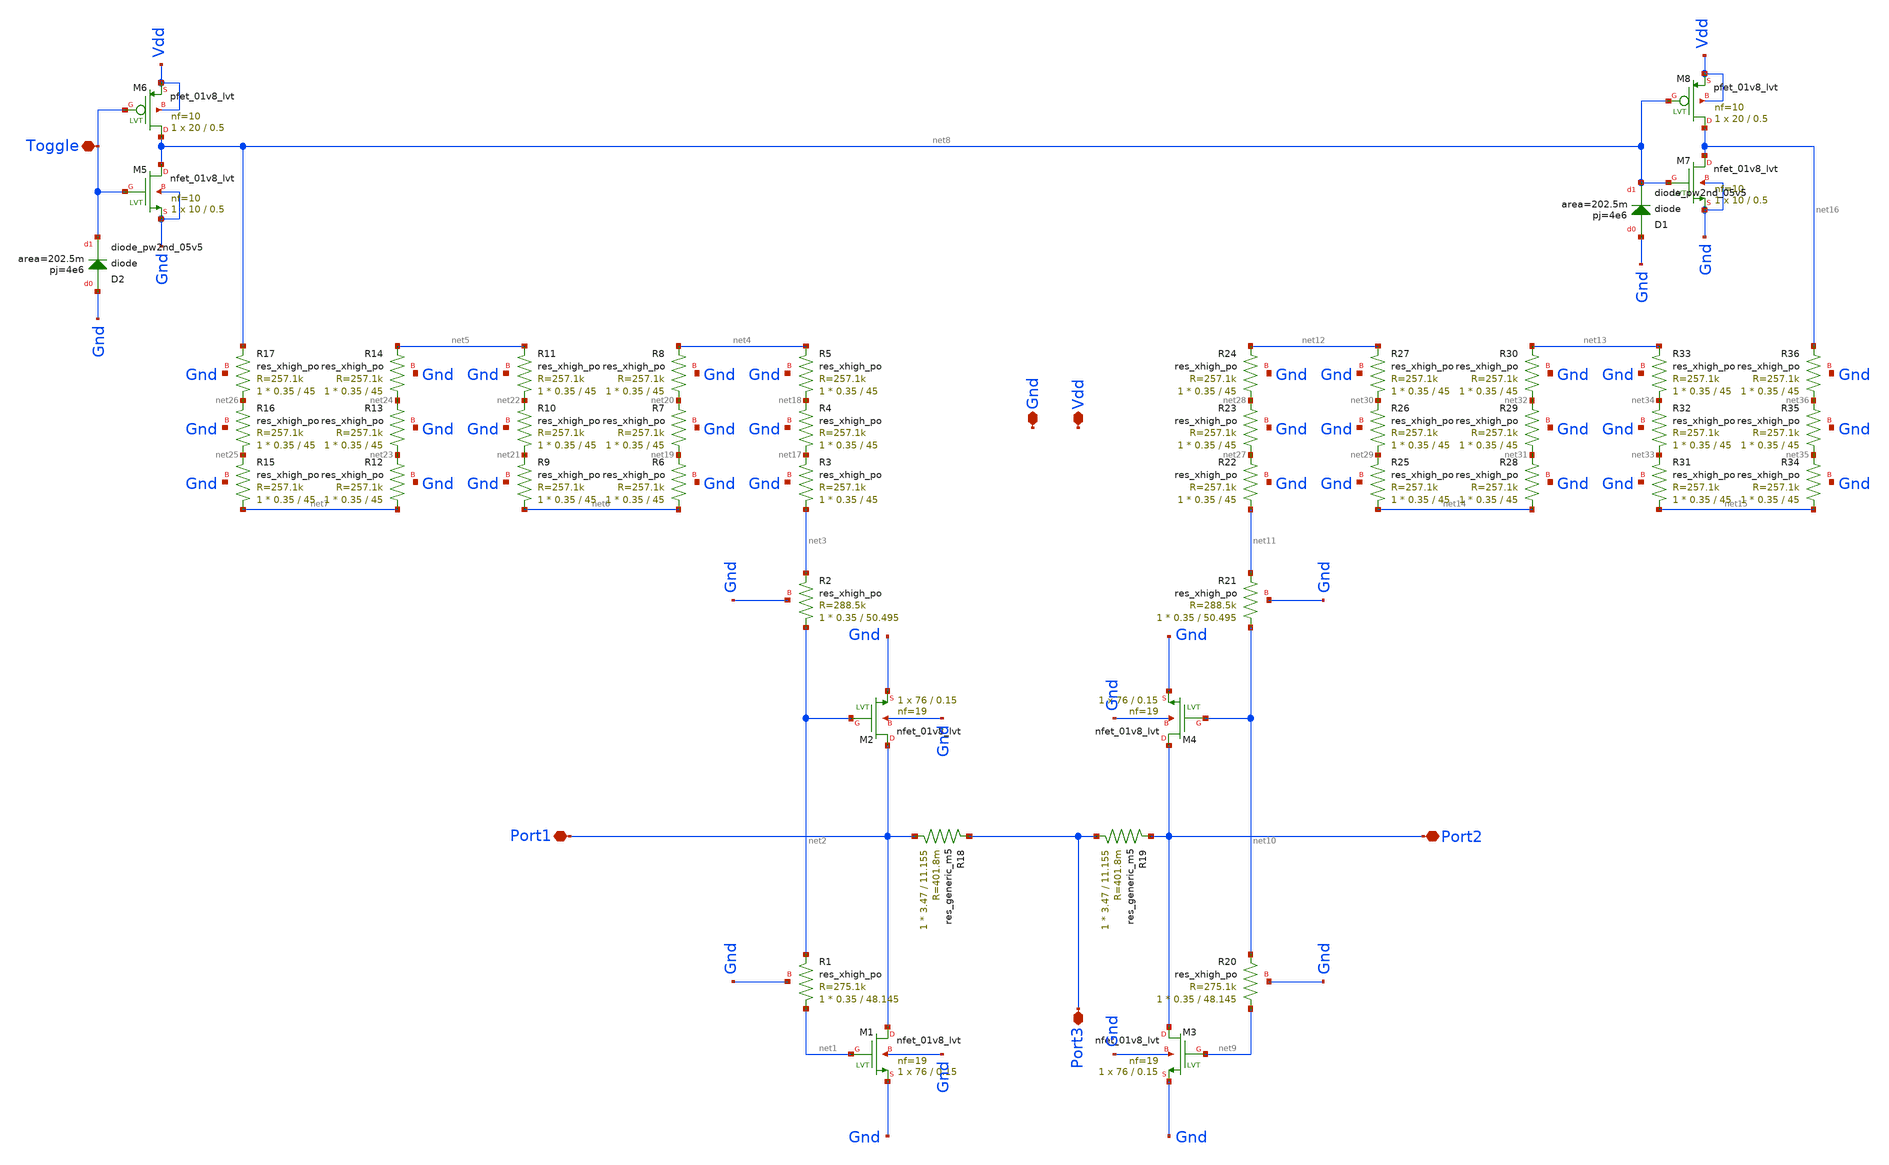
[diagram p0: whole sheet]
** sch_path: Switch_tapeout/xschem/RF_switch.sch
**.subckt RF_switch Port1 Port2 Port3 Toggle Vdd Gnd
*.iopin Port1
*.iopin Port2
*.iopin Port3
*.iopin Toggle
*.iopin Vdd
*.iopin Gnd
XM1 Port1 net1 Gnd Gnd sky130_fd_pr__nfet_01v8_lvt L=0.15 W=76 nf=19 ad='int((nf+1)/2) * W/nf * 0.29'
+ as='int((nf+2)/2) * W/nf * 0.29' pd='2*int((nf+1)/2) * (W/nf + 0.29)' ps='2*int((nf+2)/2) * (W/nf + 0.29)'
+ nrd='0.29 / W' nrs='0.29 / W' sa=0 sb=0 sd=0 mult=1 m=1
XR1 net1 net2 Gnd sky130_fd_pr__res_xhigh_po W=0.35 L=48.145 mult=1 m=1
XM2 Port1 net2 Gnd Gnd sky130_fd_pr__nfet_01v8_lvt L=0.15 W=76 nf=19 ad='int((nf+1)/2) * W/nf * 0.29'
+ as='int((nf+2)/2) * W/nf * 0.29' pd='2*int((nf+1)/2) * (W/nf + 0.29)' ps='2*int((nf+2)/2) * (W/nf + 0.29)'
+ nrd='0.29 / W' nrs='0.29 / W' sa=0 sb=0 sd=0 mult=1 m=1
XR2 net2 net3 Gnd sky130_fd_pr__res_xhigh_po W=0.35 L=50.495 mult=1 m=1
XR3 net3 net17 Gnd sky130_fd_pr__res_xhigh_po W=0.35 L=45 mult=1 m=1
XR4 net17 net18 Gnd sky130_fd_pr__res_xhigh_po W=0.35 L=45 mult=1 m=1
XR5 net18 net4 Gnd sky130_fd_pr__res_xhigh_po W=0.35 L=45 mult=1 m=1
XR6 net6 net19 Gnd sky130_fd_pr__res_xhigh_po W=0.35 L=45 mult=1 m=1
XR7 net19 net20 Gnd sky130_fd_pr__res_xhigh_po W=0.35 L=45 mult=1 m=1
XR8 net20 net4 Gnd sky130_fd_pr__res_xhigh_po W=0.35 L=45 mult=1 m=1
XR9 net6 net21 Gnd sky130_fd_pr__res_xhigh_po W=0.35 L=45 mult=1 m=1
XR10 net21 net22 Gnd sky130_fd_pr__res_xhigh_po W=0.35 L=45 mult=1 m=1
XR11 net22 net5 Gnd sky130_fd_pr__res_xhigh_po W=0.35 L=45 mult=1 m=1
XR12 net7 net23 Gnd sky130_fd_pr__res_xhigh_po W=0.35 L=45 mult=1 m=1
XR13 net23 net24 Gnd sky130_fd_pr__res_xhigh_po W=0.35 L=45 mult=1 m=1
XR14 net24 net5 Gnd sky130_fd_pr__res_xhigh_po W=0.35 L=45 mult=1 m=1
XR15 net7 net25 Gnd sky130_fd_pr__res_xhigh_po W=0.35 L=45 mult=1 m=1
XR16 net25 net26 Gnd sky130_fd_pr__res_xhigh_po W=0.35 L=45 mult=1 m=1
XR17 net26 net8 Gnd sky130_fd_pr__res_xhigh_po W=0.35 L=45 mult=1 m=1
XM3 Port2 net9 Gnd Gnd sky130_fd_pr__nfet_01v8_lvt L=0.15 W=76 nf=19 ad='int((nf+1)/2) * W/nf * 0.29'
+ as='int((nf+2)/2) * W/nf * 0.29' pd='2*int((nf+1)/2) * (W/nf + 0.29)' ps='2*int((nf+2)/2) * (W/nf + 0.29)'
+ nrd='0.29 / W' nrs='0.29 / W' sa=0 sb=0 sd=0 mult=1 m=1
XR20 net9 net10 Gnd sky130_fd_pr__res_xhigh_po W=0.35 L=48.145 mult=1 m=1
XM4 Port2 net10 Gnd Gnd sky130_fd_pr__nfet_01v8_lvt L=0.15 W=76 nf=19 ad='int((nf+1)/2) * W/nf * 0.29'
+ as='int((nf+2)/2) * W/nf * 0.29' pd='2*int((nf+1)/2) * (W/nf + 0.29)' ps='2*int((nf+2)/2) * (W/nf + 0.29)'
+ nrd='0.29 / W' nrs='0.29 / W' sa=0 sb=0 sd=0 mult=1 m=1
XR21 net10 net11 Gnd sky130_fd_pr__res_xhigh_po W=0.35 L=50.495 mult=1 m=1
XR22 net11 net27 Gnd sky130_fd_pr__res_xhigh_po W=0.35 L=45 mult=1 m=1
XR23 net27 net28 Gnd sky130_fd_pr__res_xhigh_po W=0.35 L=45 mult=1 m=1
XR24 net28 net12 Gnd sky130_fd_pr__res_xhigh_po W=0.35 L=45 mult=1 m=1
XR25 net14 net29 Gnd sky130_fd_pr__res_xhigh_po W=0.35 L=45 mult=1 m=1
XR26 net29 net30 Gnd sky130_fd_pr__res_xhigh_po W=0.35 L=45 mult=1 m=1
XR27 net30 net12 Gnd sky130_fd_pr__res_xhigh_po W=0.35 L=45 mult=1 m=1
XR28 net14 net31 Gnd sky130_fd_pr__res_xhigh_po W=0.35 L=45 mult=1 m=1
XR29 net31 net32 Gnd sky130_fd_pr__res_xhigh_po W=0.35 L=45 mult=1 m=1
XR30 net32 net13 Gnd sky130_fd_pr__res_xhigh_po W=0.35 L=45 mult=1 m=1
XR31 net15 net33 Gnd sky130_fd_pr__res_xhigh_po W=0.35 L=45 mult=1 m=1
XR32 net33 net34 Gnd sky130_fd_pr__res_xhigh_po W=0.35 L=45 mult=1 m=1
XR33 net34 net13 Gnd sky130_fd_pr__res_xhigh_po W=0.35 L=45 mult=1 m=1
XR34 net15 net35 Gnd sky130_fd_pr__res_xhigh_po W=0.35 L=45 mult=1 m=1
XR35 net35 net36 Gnd sky130_fd_pr__res_xhigh_po W=0.35 L=45 mult=1 m=1
XR36 net36 net16 Gnd sky130_fd_pr__res_xhigh_po W=0.35 L=45 mult=1 m=1
XM5 net8 Toggle Gnd Gnd sky130_fd_pr__nfet_01v8_lvt L=0.5 W=10 nf=10 ad='int((nf+1)/2) * W/nf * 0.29'
+ as='int((nf+2)/2) * W/nf * 0.29' pd='2*int((nf+1)/2) * (W/nf + 0.29)' ps='2*int((nf+2)/2) * (W/nf + 0.29)'
+ nrd='0.29 / W' nrs='0.29 / W' sa=0 sb=0 sd=0 mult=1 m=1
XM6 net8 Toggle Vdd Vdd sky130_fd_pr__pfet_01v8_lvt L=0.5 W=20 nf=10 ad='int((nf+1)/2) * W/nf * 0.29'
+ as='int((nf+2)/2) * W/nf * 0.29' pd='2*int((nf+1)/2) * (W/nf + 0.29)' ps='2*int((nf+2)/2) * (W/nf + 0.29)'
+ nrd='0.29 / W' nrs='0.29 / W' sa=0 sb=0 sd=0 mult=1 m=1
XM7 net16 net8 Gnd Gnd sky130_fd_pr__nfet_01v8_lvt L=0.5 W=10 nf=10 ad='int((nf+1)/2) * W/nf * 0.29'
+ as='int((nf+2)/2) * W/nf * 0.29' pd='2*int((nf+1)/2) * (W/nf + 0.29)' ps='2*int((nf+2)/2) * (W/nf + 0.29)'
+ nrd='0.29 / W' nrs='0.29 / W' sa=0 sb=0 sd=0 mult=1 m=1
XM8 net16 net8 Vdd Vdd sky130_fd_pr__pfet_01v8_lvt L=0.5 W=20 nf=10 ad='int((nf+1)/2) * W/nf * 0.29'
+ as='int((nf+2)/2) * W/nf * 0.29' pd='2*int((nf+1)/2) * (W/nf + 0.29)' ps='2*int((nf+2)/2) * (W/nf + 0.29)'
+ nrd='0.29 / W' nrs='0.29 / W' sa=0 sb=0 sd=0 mult=1 m=1
R18 Port1 Port3 sky130_fd_pr__res_generic_m5 W=3.47 L=11.155 m=1
R19 Port3 Port2 sky130_fd_pr__res_generic_m5 W=3.47 L=11.155 m=1
XD2 Gnd Toggle sky130_fd_pr__diode_pw2nd_05v5 area=202.5m pj=4e6
XD1 Gnd net8 sky130_fd_pr__diode_pw2nd_05v5 area=202.5m pj=4e6
**.ends
.end
